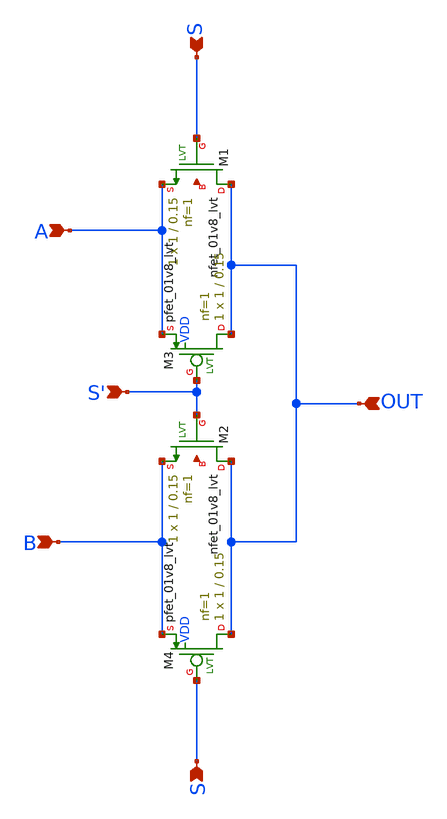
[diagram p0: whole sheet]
** sch_path: Dead_Time_Controller/multiplexer.sch
**.subckt multiplexer S S' S B A OUT
*.ipin S
*.ipin S'
*.ipin S
*.ipin B
*.ipin A
*.ipin OUT
XM1 OUT S A net1 sky130_fd_pr__nfet_01v8_lvt L=0.15 W=1 nf=1 ad='int((nf+1)/2) * W/nf * 0.29' as='int((nf+2)/2) * W/nf * 0.29'
+ pd='2*int((nf+1)/2) * (W/nf + 0.29)' ps='2*int((nf+2)/2) * (W/nf + 0.29)' nrd='0.29 / W' nrs='0.29 / W'
+ sa=0 sb=0 sd=0 mult=1 m=1
XM2 OUT S' B net2 sky130_fd_pr__nfet_01v8_lvt L=0.15 W=1 nf=1 ad='int((nf+1)/2) * W/nf * 0.29' as='int((nf+2)/2)
+ * W/nf * 0.29' pd='2*int((nf+1)/2) * (W/nf + 0.29)' ps='2*int((nf+2)/2) * (W/nf + 0.29)' nrd='0.29 /
+ W' nrs='0.29 / W' sa=0 sb=0 sd=0 mult=1 m=1
XM3 OUT S' A VDD sky130_fd_pr__pfet_01v8_lvt L=0.15 W=1 nf=1 ad='int((nf+1)/2) * W/nf * 0.29' as='int((nf+2)/2) * W/nf * 0.29'
+ pd='2*int((nf+1)/2) * (W/nf + 0.29)' ps='2*int((nf+2)/2) * (W/nf + 0.29)' nrd='0.29 / W' nrs='0.29 / W'
+ sa=0 sb=0 sd=0 mult=1 m=1
XM4 OUT S B VDD sky130_fd_pr__pfet_01v8_lvt L=0.15 W=1 nf=1 ad='int((nf+1)/2) * W/nf * 0.29' as='int((nf+2)/2) * W/nf * 0.29'
+ pd='2*int((nf+1)/2) * (W/nf + 0.29)' ps='2*int((nf+2)/2) * (W/nf + 0.29)' nrd='0.29 / W' nrs='0.29 / W'
+ sa=0 sb=0 sd=0 mult=1 m=1
**.ends
.end
